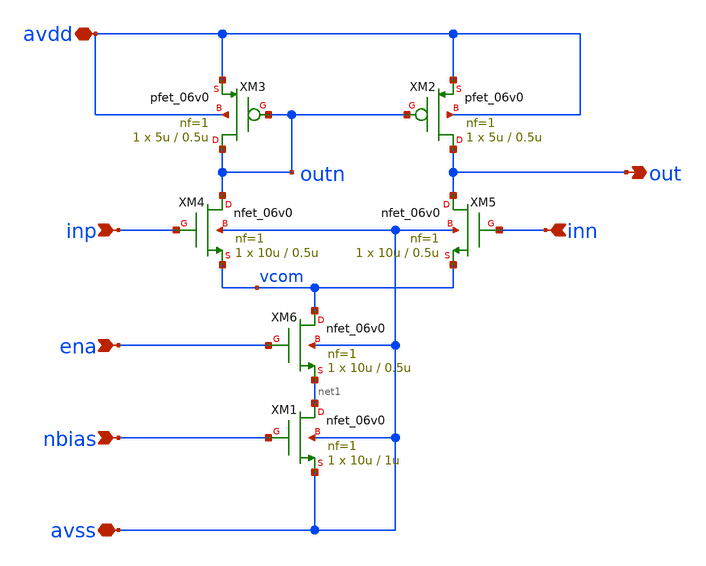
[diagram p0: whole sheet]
** sch_path: xschem/bias_amp.sch
**.subckt bias_amp inp nbias inn out avdd avss ena
*.ipin inp
*.ipin nbias
*.ipin inn
*.opin out
*.iopin avdd
*.iopin avss
*.ipin ena
XM1 net1 nbias avss avss nfet_06v0 L=1u W=10u nf=1 ad='int((nf+1)/2) * W/nf * 0.18u' as='int((nf+2)/2) * W/nf * 0.18u'
+ pd='2*int((nf+1)/2) * (W/nf + 0.18u)' ps='2*int((nf+2)/2) * (W/nf + 0.18u)' nrd='0.18u / W' nrs='0.18u / W'
+ sa=0 sb=0 sd=0 m=1 par=1
XM2 out outn avdd avdd pfet_06v0 L=0.5u W=5u nf=1 ad='int((nf+1)/2) * W/nf * 0.18u' as='int((nf+2)/2) * W/nf * 0.18u'
+ pd='2*int((nf+1)/2) * (W/nf + 0.18u)' ps='2*int((nf+2)/2) * (W/nf + 0.18u)' nrd='0.18u / W' nrs='0.18u / W'
+ sa=0 sb=0 sd=0 m=1
XM3 outn outn avdd avdd pfet_06v0 L=0.5u W=5u nf=1 ad='int((nf+1)/2) * W/nf * 0.18u' as='int((nf+2)/2) * W/nf * 0.18u'
+ pd='2*int((nf+1)/2) * (W/nf + 0.18u)' ps='2*int((nf+2)/2) * (W/nf + 0.18u)' nrd='0.18u / W' nrs='0.18u / W'
+ sa=0 sb=0 sd=0 m=1
XM4 outn inp vcom avss nfet_06v0 L=0.5u W=10u nf=1 ad='int((nf+1)/2) * W/nf * 0.18u' as='int((nf+2)/2) * W/nf * 0.18u'
+ pd='2*int((nf+1)/2) * (W/nf + 0.18u)' ps='2*int((nf+2)/2) * (W/nf + 0.18u)' nrd='0.18u / W' nrs='0.18u / W'
+ sa=0 sb=0 sd=0 m=1 par=1
XM5 out inn vcom avss nfet_06v0 L=0.5u W=10u nf=1 ad='int((nf+1)/2) * W/nf * 0.18u' as='int((nf+2)/2) * W/nf * 0.18u'
+ pd='2*int((nf+1)/2) * (W/nf + 0.18u)' ps='2*int((nf+2)/2) * (W/nf + 0.18u)' nrd='0.18u / W' nrs='0.18u / W'
+ sa=0 sb=0 sd=0 m=1 par=1
XM6 vcom ena net1 avss nfet_06v0 L=0.5u W=10u nf=1 ad='int((nf+1)/2) * W/nf * 0.18u' as='int((nf+2)/2) * W/nf * 0.18u'
+ pd='2*int((nf+1)/2) * (W/nf + 0.18u)' ps='2*int((nf+2)/2) * (W/nf + 0.18u)' nrd='0.18u / W' nrs='0.18u / W'
+ sa=0 sb=0 sd=0 m=1 par=1
**.ends
.end
